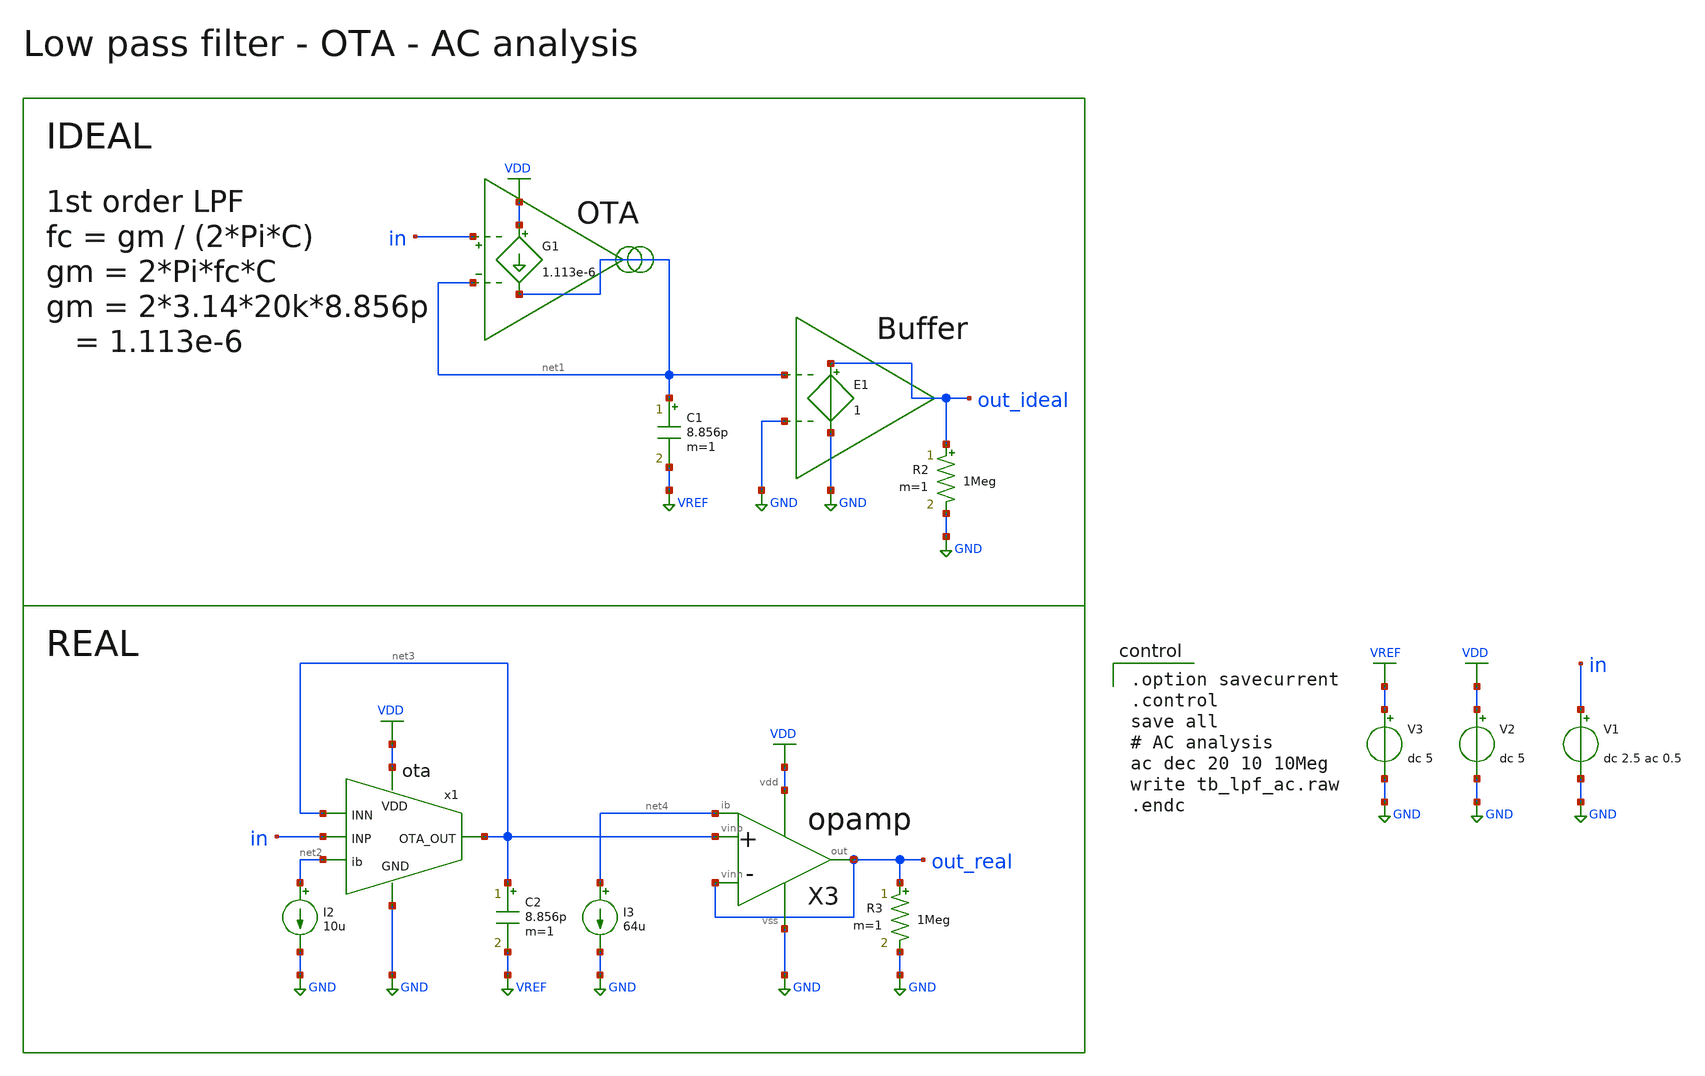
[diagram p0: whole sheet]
** sch_path: member_project/AM_Radio/Yamada3/xschem/tb_lpf_ac.sch
**.subckt tb_lpf_ac
V2 VDD GND dc 5
V1 in GND dc 2.5 ac 0.5
G1 VDD net1 in net1 1.113e-6
C1 net1 VREF 8.856p m=1
E1 out_ideal GND net1 GND 1
x1 VDD net2 net3 in net3 GND ota
I2 net2 GND 10u
C2 net3 VREF 8.856p m=1
V3 VREF GND dc 5
R2 out_ideal GND 1Meg m=1
I3 net4 GND 64u
R3 out_real GND 1Meg m=1
X3 net3 out_real net4 out_real VDD GND opamp
**** begin user architecture code

.option savecurrent
.control
save all
# AC analysis
ac dec 20 10 10Meg
write tb_lpf_ac.raw
.endc

 .include $::LIB/ip62_models
**** end user architecture code
**.ends
.GLOBAL GND
.GLOBAL VDD
.GLOBAL VREF
.end
